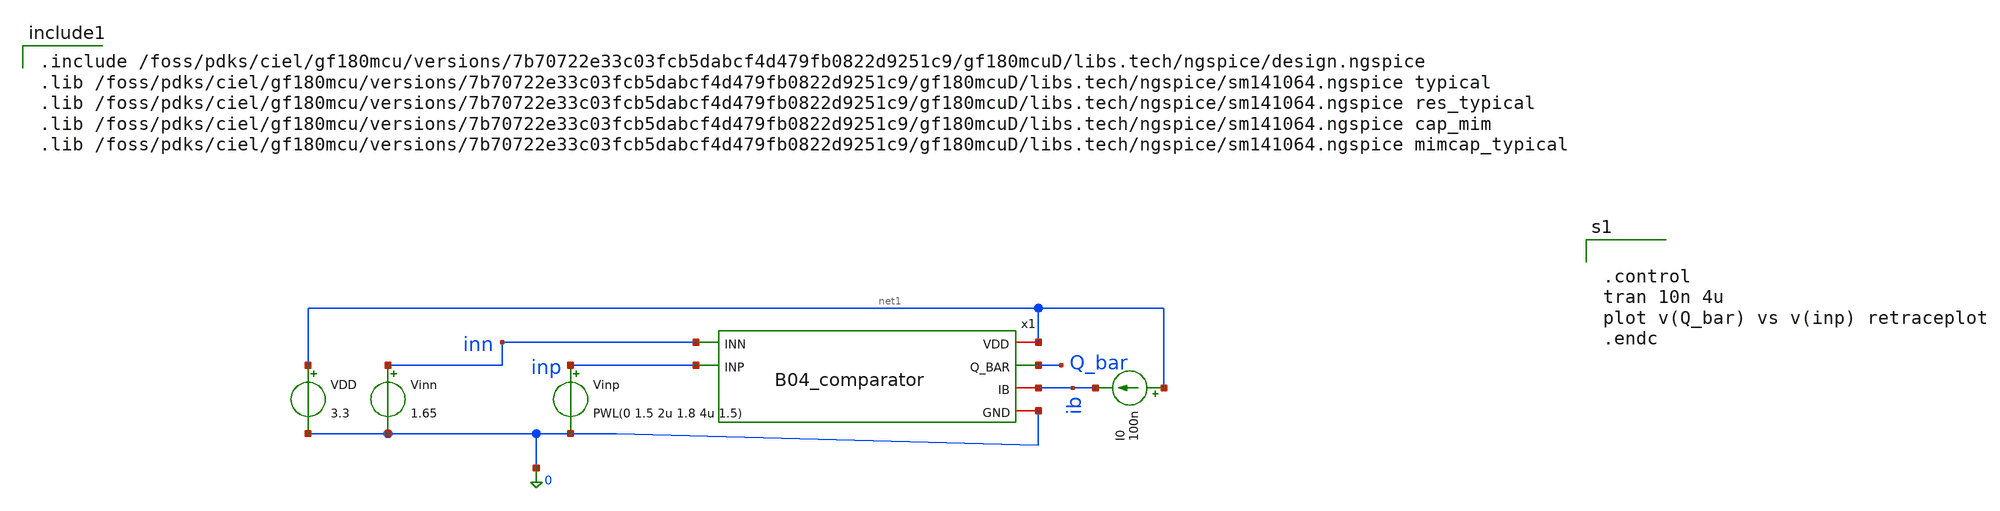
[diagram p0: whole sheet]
** sch_path: analog/B04_tb_comparator.sch
**.subckt B04_tb_comparator
Vinn inn 0 1.65
VDD net1 0 3.3
Vinp inp 0 PWL(0 1.5 2u 1.8 4u 1.5)
I0 net1 ib 100n
x1 net1 Q_bar inn inp ib 0 B04_comparator
**** begin user architecture code

.include /foss/pdks/ciel/gf180mcu/versions/7b70722e33c03fcb5dabcf4d479fb0822d9251c9/gf180mcuD/libs.tech/ngspice/design.ngspice
.lib /foss/pdks/ciel/gf180mcu/versions/7b70722e33c03fcb5dabcf4d479fb0822d9251c9/gf180mcuD/libs.tech/ngspice/sm141064.ngspice typical
.lib /foss/pdks/ciel/gf180mcu/versions/7b70722e33c03fcb5dabcf4d479fb0822d9251c9/gf180mcuD/libs.tech/ngspice/sm141064.ngspice res_typical
.lib /foss/pdks/ciel/gf180mcu/versions/7b70722e33c03fcb5dabcf4d479fb0822d9251c9/gf180mcuD/libs.tech/ngspice/sm141064.ngspice cap_mim
.lib /foss/pdks/ciel/gf180mcu/versions/7b70722e33c03fcb5dabcf4d479fb0822d9251c9/gf180mcuD/libs.tech/ngspice/sm141064.ngspice mimcap_typical



.control
tran 10n 4u
plot v(Q_bar) vs v(inp) retraceplot
.endc


**** end user architecture code
**.ends
.end
